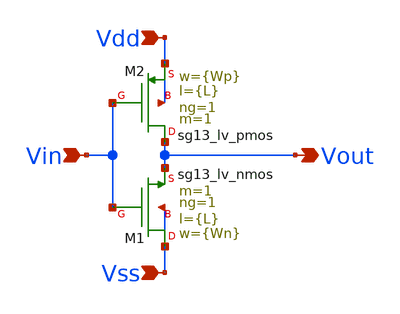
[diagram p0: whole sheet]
** sch_path: Taller1/Insumos/inv_lv.sch
**.subckt inv_lv Vdd Vss Vin Vout
*.ipin Vdd
*.ipin Vss
*.ipin Vin
*.opin Vout
XM1 Vss Vin Vout Vss sg13_lv_nmos w={Wn} l={L} ng=1 m=1 mm_ok=1
XM2 Vout Vin Vdd Vdd sg13_lv_pmos w={Wp} l={L} ng=1 m=1 mm_ok=1
**.ends
.end
